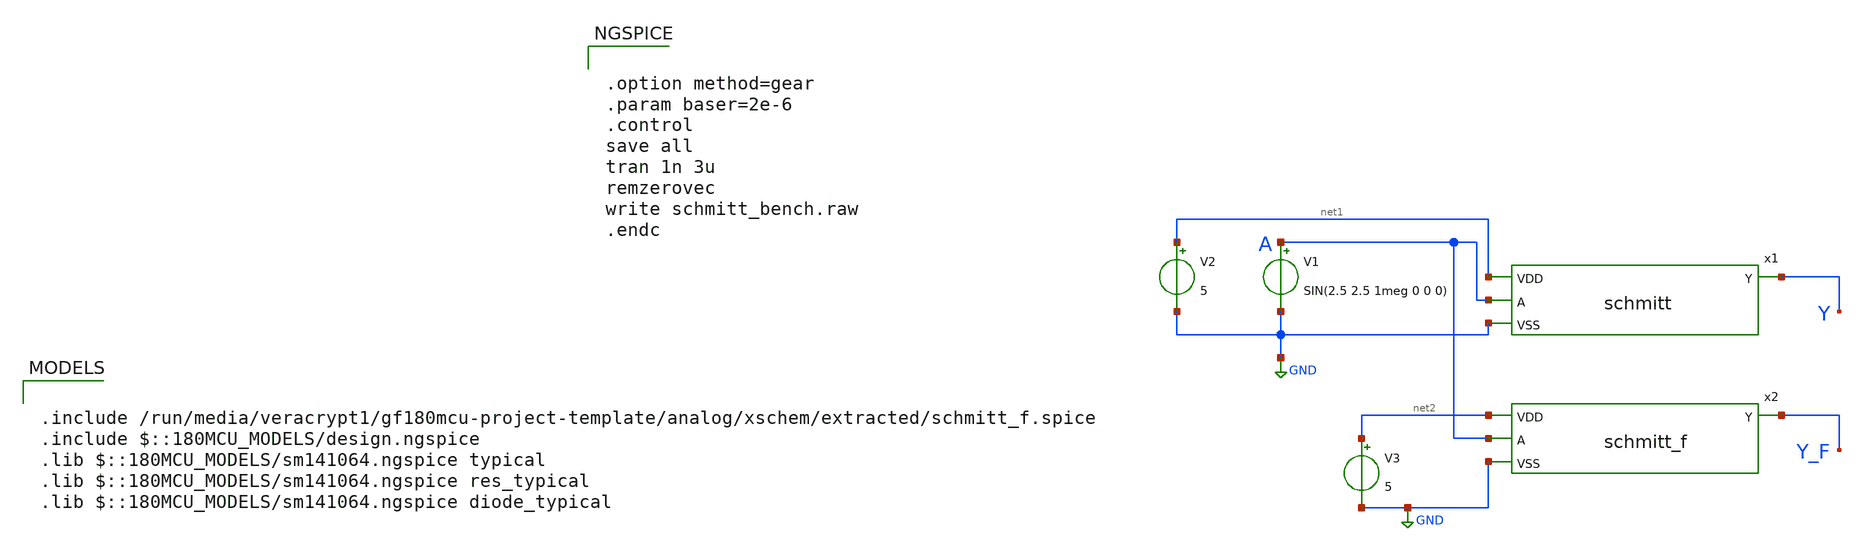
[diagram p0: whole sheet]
** sch_path: analog/xschem/schmitt_bench.sch
**.subckt schmitt_bench
V1 A GND SIN(2.5 2.5 1meg 0 0 0)
V2 net1 GND 5
x1 net1 A Y GND schmitt
x2 net2 GND A Y_F schmitt_f
V3 net2 GND 5
**** begin user architecture code


.option method=gear
.param baser=2e-6
.control
save all
tran 1n 3u
remzerovec
write schmitt_bench.raw
.endc



.include /run/media/veracrypt1/gf180mcu-project-template/analog/xschem/extracted/schmitt_f.spice
.include $::180MCU_MODELS/design.ngspice
.lib $::180MCU_MODELS/sm141064.ngspice typical
.lib $::180MCU_MODELS/sm141064.ngspice res_typical
.lib $::180MCU_MODELS/sm141064.ngspice diode_typical

**** end user architecture code
**.ends

* expanding   symbol:  schmitt.sym # of pins=4
** sym_path: analog/xschem/schmitt.sym
** sch_path: analog/xschem/schmitt.sch
.subckt schmitt VDD A Y VSS
*.ipin VDD
*.ipin VSS
*.ipin A
*.opin Y
XM1 net1 A VDD VDD pfet_06v0 L=0.55u W=4u nf=1 ad='int((nf+1)/2) * W/nf * 0.18u' as='int((nf+2)/2) * W/nf * 0.18u'
+ pd='2*int((nf+1)/2) * (W/nf + 0.18u)' ps='2*int((nf+2)/2) * (W/nf + 0.18u)' nrd='0.18u / W' nrs='0.18u / W'
+ sa=0 sb=0 sd=0 m=1
XM2 Y A net1 VDD pfet_06v0 L=0.55u W=4u nf=1 ad='int((nf+1)/2) * W/nf * 0.18u' as='int((nf+2)/2) * W/nf * 0.18u'
+ pd='2*int((nf+1)/2) * (W/nf + 0.18u)' ps='2*int((nf+2)/2) * (W/nf + 0.18u)' nrd='0.18u / W' nrs='0.18u / W'
+ sa=0 sb=0 sd=0 m=1
XM3 Y A net2 VSS nfet_06v0 L=0.70u W=4u nf=1 ad='int((nf+1)/2) * W/nf * 0.18u' as='int((nf+2)/2) * W/nf * 0.18u'
+ pd='2*int((nf+1)/2) * (W/nf + 0.18u)' ps='2*int((nf+2)/2) * (W/nf + 0.18u)' nrd='0.18u / W' nrs='0.18u / W'
+ sa=0 sb=0 sd=0 m=1
XM4 net2 A VSS VSS nfet_06v0 L=0.70u W=4u nf=1 ad='int((nf+1)/2) * W/nf * 0.18u' as='int((nf+2)/2) * W/nf * 0.18u'
+ pd='2*int((nf+1)/2) * (W/nf + 0.18u)' ps='2*int((nf+2)/2) * (W/nf + 0.18u)' nrd='0.18u / W' nrs='0.18u / W'
+ sa=0 sb=0 sd=0 m=1
XM5 VSS Y net1 VDD pfet_06v0 L=0.55u W=2u nf=1 ad='int((nf+1)/2) * W/nf * 0.18u' as='int((nf+2)/2) * W/nf * 0.18u'
+ pd='2*int((nf+1)/2) * (W/nf + 0.18u)' ps='2*int((nf+2)/2) * (W/nf + 0.18u)' nrd='0.18u / W' nrs='0.18u / W'
+ sa=0 sb=0 sd=0 m=1
XM6 VDD Y net2 VSS nfet_06v0 L=0.70u W=2u nf=1 ad='int((nf+1)/2) * W/nf * 0.18u' as='int((nf+2)/2) * W/nf * 0.18u'
+ pd='2*int((nf+1)/2) * (W/nf + 0.18u)' ps='2*int((nf+2)/2) * (W/nf + 0.18u)' nrd='0.18u / W' nrs='0.18u / W'
+ sa=0 sb=0 sd=0 m=1
.ends

.GLOBAL GND
.end
